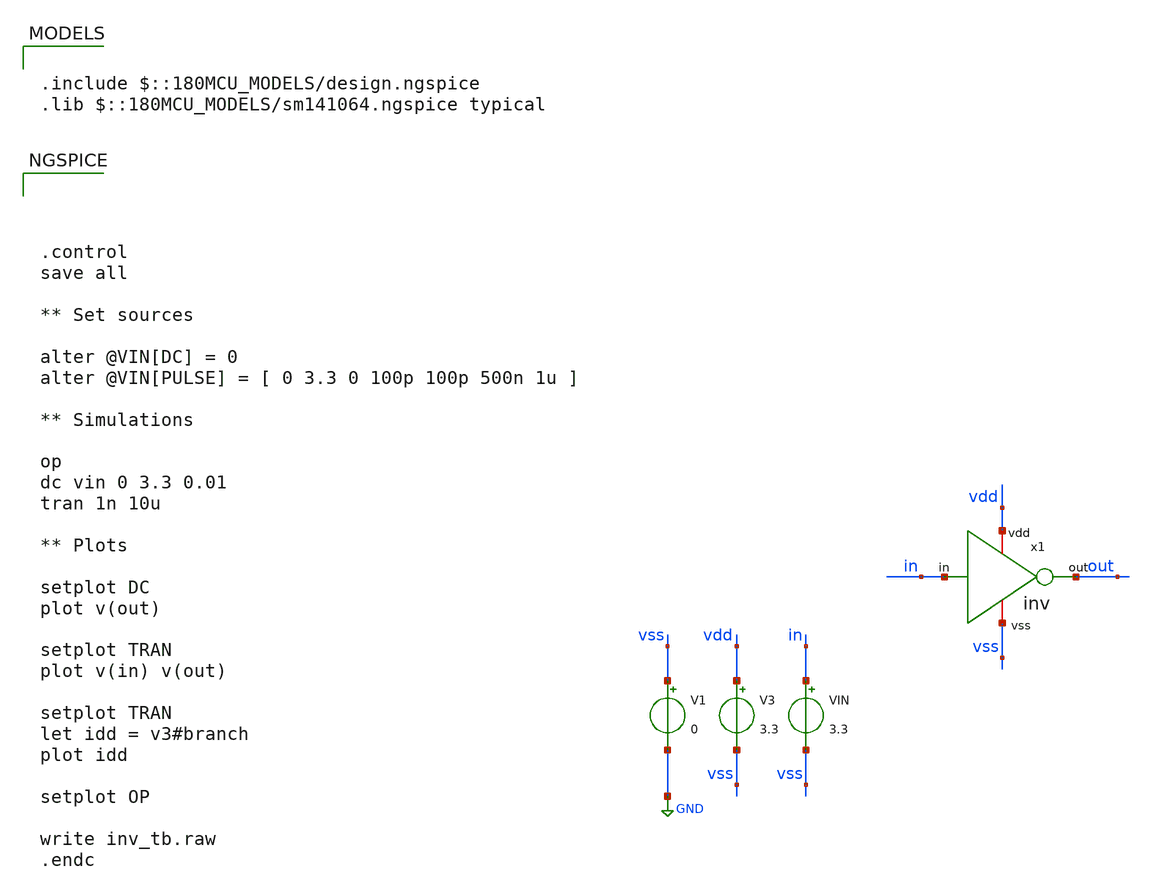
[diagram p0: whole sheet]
** sch_path: DESIGN/DACFUTURE_EDU/inv/inv_tb.sch
**.subckt inv_tb
V1 vss GND 0
V3 vdd vss 3.3
VIN in vss 3.3
.save i(vin)
x1 in out vdd vss inv
**** begin user architecture code

.include $::180MCU_MODELS/design.ngspice
.lib $::180MCU_MODELS/sm141064.ngspice typical





.control
save all

** Set sources

alter @VIN[DC] = 0
alter @VIN[PULSE] = [ 0 3.3 0 100p 100p 500n 1u ]

** Simulations

op
dc vin 0 3.3 0.01
tran 1n 10u

** Plots

setplot DC
plot v(out)

setplot TRAN
plot v(in) v(out)

setplot TRAN
let idd = v3#branch
plot idd

setplot OP

write inv_tb.raw
.endc


**** end user architecture code
**.ends
.GLOBAL GND
.end
